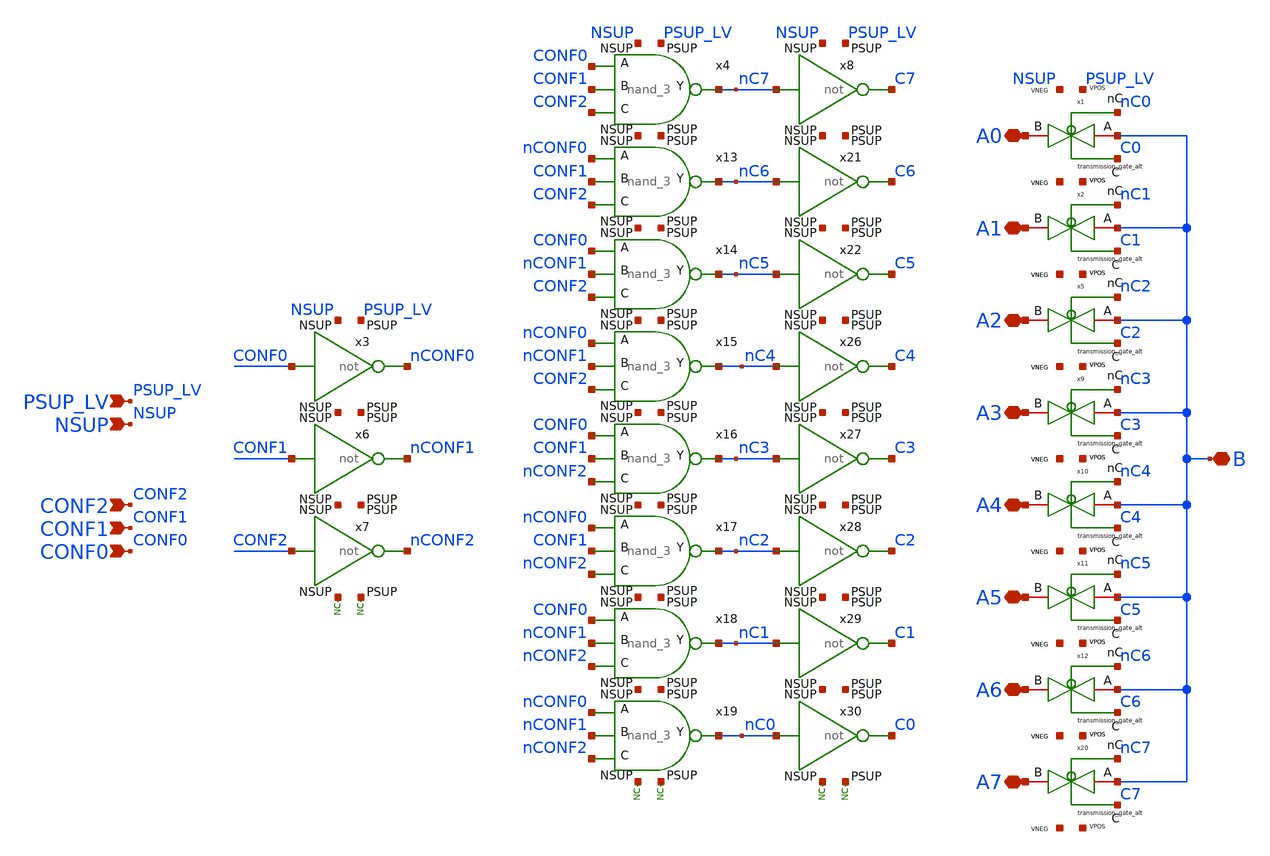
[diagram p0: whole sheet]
** sch_path: xschem/blocks/mux_3/mux_3.sch
**.subckt mux_3 PSUP_LV NSUP CONF1 CONF2 CONF0 A0 A1 A2 A3 A4 A5 A6 A7 B
*.ipin PSUP_LV
*.ipin NSUP
*.ipin CONF1
*.ipin CONF2
*.ipin CONF0
*.iopin A0
*.iopin A1
*.iopin A2
*.iopin A3
*.iopin A4
*.iopin A5
*.iopin A6
*.iopin A7
*.iopin B
x13 nC6 nCONF0 CONF2 PSUP_LV NSUP CONF1 nand_3
x14 nC5 CONF0 CONF2 PSUP_LV NSUP nCONF1 nand_3
x15 nC4 nCONF0 CONF2 PSUP_LV NSUP nCONF1 nand_3
x16 nC3 CONF0 nCONF2 PSUP_LV NSUP CONF1 nand_3
x17 nC2 nCONF0 nCONF2 PSUP_LV NSUP CONF1 nand_3
x18 nC1 CONF0 nCONF2 PSUP_LV NSUP nCONF1 nand_3
x19 nC0 nCONF0 nCONF2 PSUP_LV NSUP nCONF1 nand_3
* noconn NSUP
* noconn PSUP_LV
x21 PSUP_LV nC6 C6 NSUP not
x22 PSUP_LV nC5 C5 NSUP not
* noconn NSUP
* noconn PSUP_LV
x26 PSUP_LV nC4 C4 NSUP not
x27 PSUP_LV nC3 C3 NSUP not
x28 PSUP_LV nC2 C2 NSUP not
x29 PSUP_LV nC1 C1 NSUP not
x30 PSUP_LV nC0 C0 NSUP not
* noconn NSUP
* noconn PSUP_LV
x3 PSUP_LV CONF0 nCONF0 NSUP not
x6 PSUP_LV CONF1 nCONF1 NSUP not
x7 PSUP_LV CONF2 nCONF2 NSUP not
x4 nC7 CONF0 CONF2 PSUP_LV NSUP CONF1 nand_3
x8 PSUP_LV nC7 C7 NSUP not
x1 C0 B A0 nC0 PSUP_LV NSUP transmission_gate_alt
x2 C1 B A1 nC1 PSUP_LV NSUP transmission_gate_alt
x5 C2 B A2 nC2 PSUP_LV NSUP transmission_gate_alt
x9 C3 B A3 nC3 PSUP_LV NSUP transmission_gate_alt
x10 C4 B A4 nC4 PSUP_LV NSUP transmission_gate_alt
x11 C5 B A5 nC5 PSUP_LV NSUP transmission_gate_alt
x12 C6 B A6 nC6 PSUP_LV NSUP transmission_gate_alt
x20 C7 B A7 nC7 PSUP_LV NSUP transmission_gate_alt
**.ends

* expanding   symbol:  blocks/nand_3/nand_3.sym # of pins=8
** sym_path: xschem/blocks/nand_3/nand_3.sym
** sch_path: xschem/blocks/nand_3/nand_3.sch
.subckt nand_3 Y A C PSUP NSUP B
*.ipin PSUP
*.ipin NSUP
*.ipin A
*.ipin B
*.opin Y
*.ipin C
XM5 net1 C NSUP NSUP nfet_03v3 L=0.28u W=0.22u nf=1 ad='int((nf+1)/2) * W/nf * 0.18u' as='int((nf+2)/2) * W/nf * 0.18u'
+ pd='2*int((nf+1)/2) * (W/nf + 0.18u)' ps='2*int((nf+2)/2) * (W/nf + 0.18u)' nrd='0.18u / W' nrs='0.18u / W'
+ sa=0 sb=0 sd=0 m=1
XM1 Y A net2 NSUP nfet_03v3 L=0.28u W=0.22u nf=1 ad='int((nf+1)/2) * W/nf * 0.18u' as='int((nf+2)/2) * W/nf * 0.18u'
+ pd='2*int((nf+1)/2) * (W/nf + 0.18u)' ps='2*int((nf+2)/2) * (W/nf + 0.18u)' nrd='0.18u / W' nrs='0.18u / W'
+ sa=0 sb=0 sd=0 m=1
XM2 Y C PSUP PSUP pfet_03v3 L=0.28u W=0.5u nf=1 ad='int((nf+1)/2) * W/nf * 0.18u' as='int((nf+2)/2) * W/nf * 0.18u'
+ pd='2*int((nf+1)/2) * (W/nf + 0.18u)' ps='2*int((nf+2)/2) * (W/nf + 0.18u)' nrd='0.18u / W' nrs='0.18u / W'
+ sa=0 sb=0 sd=0 m=1
XM3 Y B PSUP PSUP pfet_03v3 L=0.28u W=0.5u nf=1 ad='int((nf+1)/2) * W/nf * 0.18u' as='int((nf+2)/2) * W/nf * 0.18u'
+ pd='2*int((nf+1)/2) * (W/nf + 0.18u)' ps='2*int((nf+2)/2) * (W/nf + 0.18u)' nrd='0.18u / W' nrs='0.18u / W'
+ sa=0 sb=0 sd=0 m=1
XM4 net2 B net1 NSUP nfet_03v3 L=0.28u W=0.22u nf=1 ad='int((nf+1)/2) * W/nf * 0.18u' as='int((nf+2)/2) * W/nf * 0.18u'
+ pd='2*int((nf+1)/2) * (W/nf + 0.18u)' ps='2*int((nf+2)/2) * (W/nf + 0.18u)' nrd='0.18u / W' nrs='0.18u / W'
+ sa=0 sb=0 sd=0 m=1
XM6 Y A PSUP PSUP pfet_03v3 L=0.28u W=0.5u nf=1 ad='int((nf+1)/2) * W/nf * 0.18u' as='int((nf+2)/2) * W/nf * 0.18u'
+ pd='2*int((nf+1)/2) * (W/nf + 0.18u)' ps='2*int((nf+2)/2) * (W/nf + 0.18u)' nrd='0.18u / W' nrs='0.18u / W'
+ sa=0 sb=0 sd=0 m=1
.ends


* expanding   symbol:  blocks/not/not.sym # of pins=6
** sym_path: xschem/blocks/not/not.sym
** sch_path: xschem/blocks/not/not.sch
.subckt not PSUP A B NSUP
*.ipin PSUP
*.ipin NSUP
*.ipin A
*.opin B
XM2 B A NSUP NSUP nfet_03v3 L=0.28u W=0.22u nf=1 ad='int((nf+1)/2) * W/nf * 0.18u' as='int((nf+2)/2) * W/nf * 0.18u'
+ pd='2*int((nf+1)/2) * (W/nf + 0.18u)' ps='2*int((nf+2)/2) * (W/nf + 0.18u)' nrd='0.18u / W' nrs='0.18u / W'
+ sa=0 sb=0 sd=0 m=1
XM1 B A PSUP PSUP pfet_03v3 L=0.28u W=0.5u nf=1 ad='int((nf+1)/2) * W/nf * 0.18u' as='int((nf+2)/2) * W/nf * 0.18u'
+ pd='2*int((nf+1)/2) * (W/nf + 0.18u)' ps='2*int((nf+2)/2) * (W/nf + 0.18u)' nrd='0.18u / W' nrs='0.18u / W'
+ sa=0 sb=0 sd=0 m=1
.ends


* expanding   symbol:  blocks/transmission_gate/transmission_gate_alt.sym # of pins=8
** sym_path: xschem/blocks/transmission_gate/transmission_gate_alt.sym
** sch_path: xschem/blocks/transmission_gate/transmission_gate_alt.sch
.subckt transmission_gate_alt C A B nC VPOS VNEG
*.iopin A
*.iopin B
*.ipin C
*.ipin nC
*.ipin VPOS
*.ipin VNEG
x1 C A B nC VPOS VNEG transmission_gate
.ends


* expanding   symbol:  blocks/transmission_gate/transmission_gate.sym # of pins=6
** sym_path: xschem/blocks/transmission_gate/transmission_gate.sym
** sch_path: xschem/blocks/transmission_gate/transmission_gate.sch
.subckt transmission_gate C A B nC VPOS VNEG
*.iopin A
*.iopin B
*.ipin C
*.ipin nC
*.ipin VPOS
*.ipin VNEG
XM3 A C B VNEG nfet_03v3 L=2u W=10u nf=1 ad='int((nf+1)/2) * W/nf * 0.18u' as='int((nf+2)/2) * W/nf * 0.18u'
+ pd='2*int((nf+1)/2) * (W/nf + 0.18u)' ps='2*int((nf+2)/2) * (W/nf + 0.18u)' nrd='0.18u / W' nrs='0.18u / W'
+ sa=0 sb=0 sd=0 m=2
XM4 A nC B VPOS pfet_03v3 L=2u W=10u nf=1 ad='int((nf+1)/2) * W/nf * 0.18u' as='int((nf+2)/2) * W/nf * 0.18u'
+ pd='2*int((nf+1)/2) * (W/nf + 0.18u)' ps='2*int((nf+2)/2) * (W/nf + 0.18u)' nrd='0.18u / W' nrs='0.18u / W'
+ sa=0 sb=0 sd=0 m=4
.ends

.end
